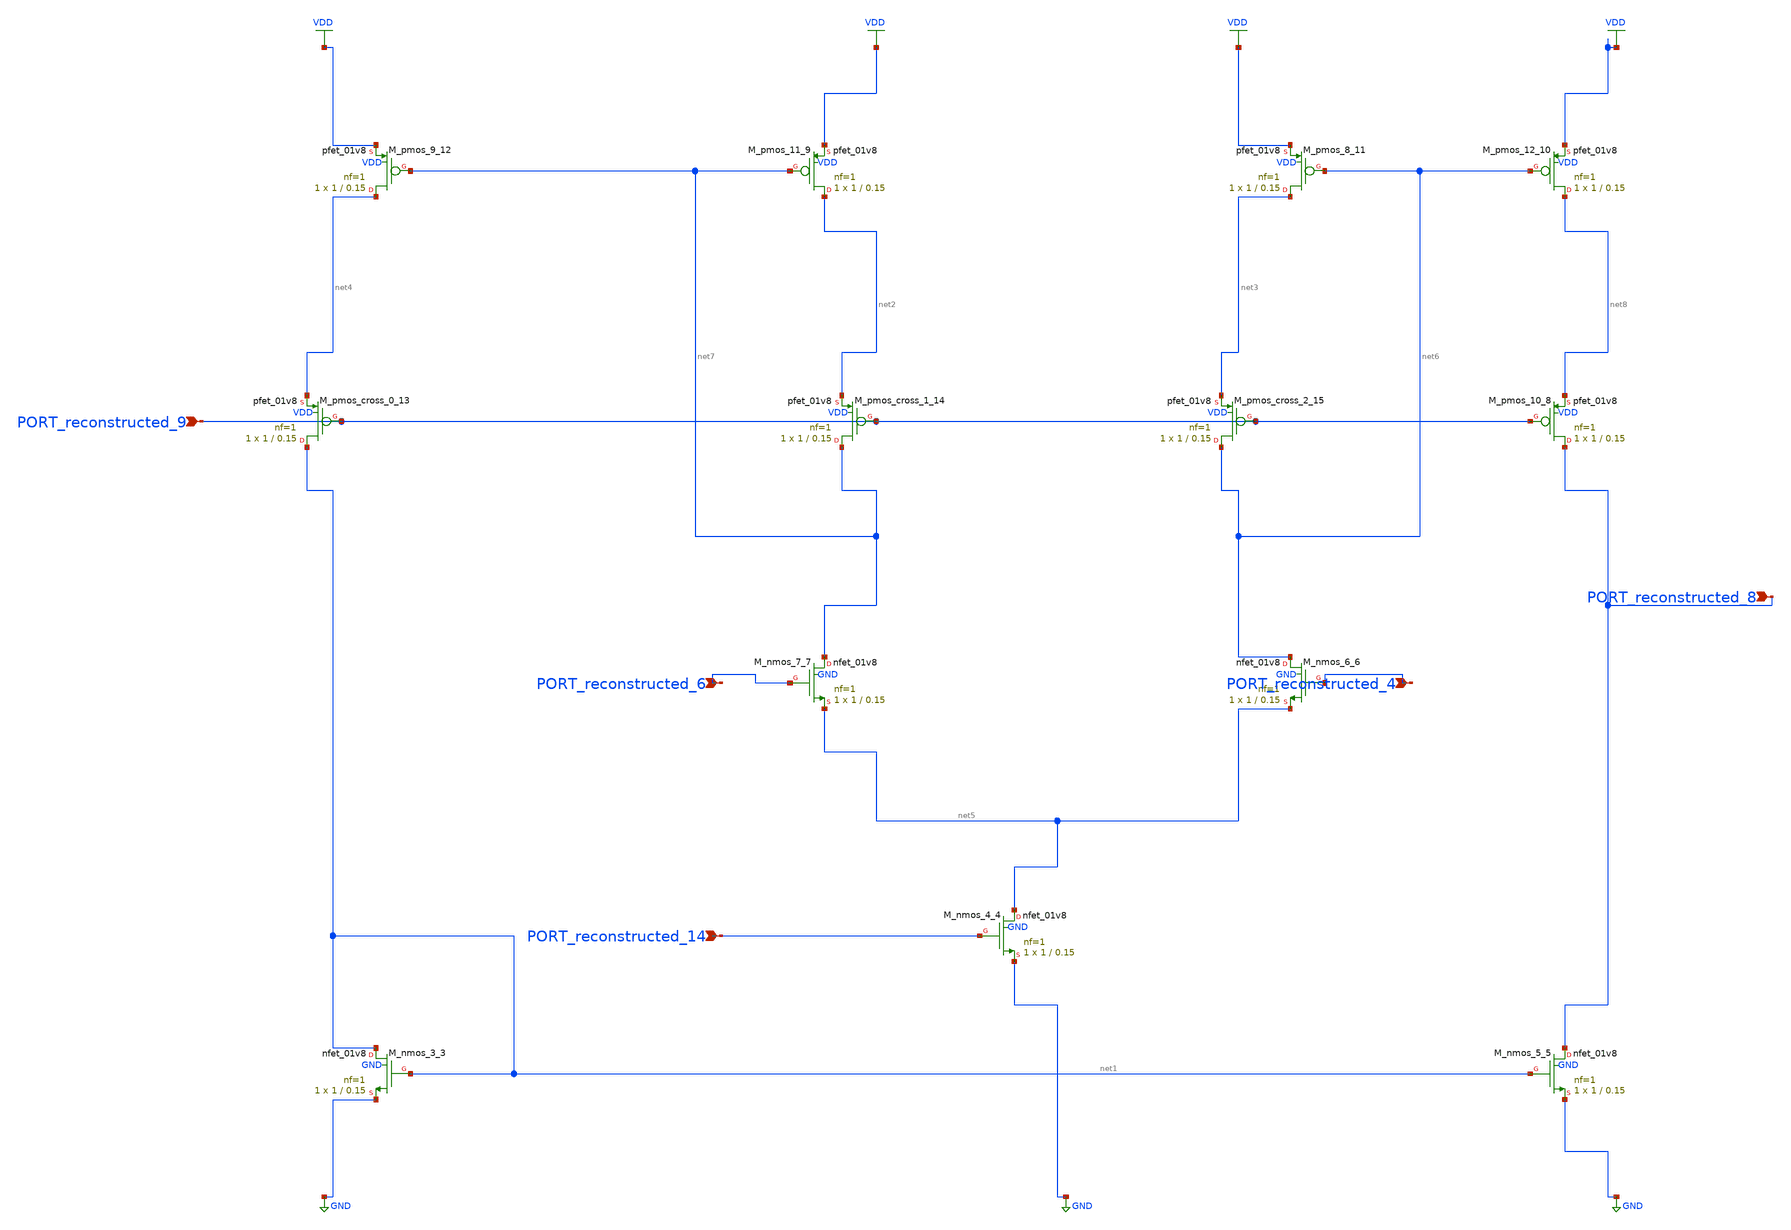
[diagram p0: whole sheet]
** sch_path: schematics/10_1007_BF02104746_102_002.sch
**.subckt 10_1007_BF02104746_102_002 PORT_reconstructed_6 PORT_reconstructed_8 PORT_reconstructed_14
*+ PORT_reconstructed_4 PORT_reconstructed_9
*.ipin PORT_reconstructed_6
*.ipin PORT_reconstructed_8
*.ipin PORT_reconstructed_14
*.ipin PORT_reconstructed_4
*.ipin PORT_reconstructed_9
XM_nmos_3_3 net1 net1 GND GND sky130_fd_pr__nfet_01v8 L=0.15 W=1 nf=1 ad='int((1 + 1)/2) * 1 / 1 * 0.29'
+ as='int((1 + 2)/2) * 1 / 1 * 0.29' pd='2*int((1 + 1)/2) * (1 / 1 + 0.29)' ps='2*int((1 + 2)/2) * (1 / 1 + 0.29)'
+ nrd='0.29 / 1 ' nrs='0.29 / 1 ' sa=0 sb=0 sd=0 mult=1 m=1
XM_nmos_4_4 net5 PORT_reconstructed_14 GND GND sky130_fd_pr__nfet_01v8 L=0.15 W=1 nf=1 ad='int((1 + 1)/2) * 1 / 1 * 0.29'
+ as='int((1 + 2)/2) * 1 / 1 * 0.29' pd='2*int((1 + 1)/2) * (1 / 1 + 0.29)' ps='2*int((1 + 2)/2) * (1 / 1 + 0.29)'
+ nrd='0.29 / 1 ' nrs='0.29 / 1 ' sa=0 sb=0 sd=0 mult=1 m=1
XM_nmos_5_5 PORT_reconstructed_8 net1 GND GND sky130_fd_pr__nfet_01v8 L=0.15 W=1 nf=1 ad='int((1 + 1)/2) * 1 / 1 * 0.29'
+ as='int((1 + 2)/2) * 1 / 1 * 0.29' pd='2*int((1 + 1)/2) * (1 / 1 + 0.29)' ps='2*int((1 + 2)/2) * (1 / 1 + 0.29)'
+ nrd='0.29 / 1 ' nrs='0.29 / 1 ' sa=0 sb=0 sd=0 mult=1 m=1
XM_nmos_6_6 net6 PORT_reconstructed_4 net5 GND sky130_fd_pr__nfet_01v8 L=0.15 W=1 nf=1 ad='int((1 + 1)/2) * 1 / 1 * 0.29'
+ as='int((1 + 2)/2) * 1 / 1 * 0.29' pd='2*int((1 + 1)/2) * (1 / 1 + 0.29)' ps='2*int((1 + 2)/2) * (1 / 1 + 0.29)'
+ nrd='0.29 / 1 ' nrs='0.29 / 1 ' sa=0 sb=0 sd=0 mult=1 m=1
XM_nmos_7_7 net7 PORT_reconstructed_6 net5 GND sky130_fd_pr__nfet_01v8 L=0.15 W=1 nf=1 ad='int((1 + 1)/2) * 1 / 1 * 0.29'
+ as='int((1 + 2)/2) * 1 / 1 * 0.29' pd='2*int((1 + 1)/2) * (1 / 1 + 0.29)' ps='2*int((1 + 2)/2) * (1 / 1 + 0.29)'
+ nrd='0.29 / 1 ' nrs='0.29 / 1 ' sa=0 sb=0 sd=0 mult=1 m=1
XM_pmos_10_8 PORT_reconstructed_8 PORT_reconstructed_9 net8 VDD sky130_fd_pr__pfet_01v8 L=0.15 W=1 nf=1
+ ad='int((1 + 1)/2) * 1 / 1 * 0.29' as='int((1 + 2)/2) * 1 / 1 * 0.29' pd='2*int((1 + 1)/2) * (1 / 1 + 0.29)'
+ ps='2*int((1 + 2)/2) * (1 / 1 + 0.29)' nrd='0.29 / 1 ' nrs='0.29 / 1 ' sa=0 sb=0 sd=0 mult=1 m=1
XM_pmos_11_9 net2 net7 VDD VDD sky130_fd_pr__pfet_01v8 L=0.15 W=1 nf=1 ad='int((1 + 1)/2) * 1 / 1 * 0.29'
+ as='int((1 + 2)/2) * 1 / 1 * 0.29' pd='2*int((1 + 1)/2) * (1 / 1 + 0.29)' ps='2*int((1 + 2)/2) * (1 / 1 + 0.29)'
+ nrd='0.29 / 1 ' nrs='0.29 / 1 ' sa=0 sb=0 sd=0 mult=1 m=1
XM_pmos_12_10 net8 net6 VDD VDD sky130_fd_pr__pfet_01v8 L=0.15 W=1 nf=1 ad='int((1 + 1)/2) * 1 / 1 * 0.29'
+ as='int((1 + 2)/2) * 1 / 1 * 0.29' pd='2*int((1 + 1)/2) * (1 / 1 + 0.29)' ps='2*int((1 + 2)/2) * (1 / 1 + 0.29)'
+ nrd='0.29 / 1 ' nrs='0.29 / 1 ' sa=0 sb=0 sd=0 mult=1 m=1
XM_pmos_8_11 net3 net6 VDD VDD sky130_fd_pr__pfet_01v8 L=0.15 W=1 nf=1 ad='int((1 + 1)/2) * 1 / 1 * 0.29'
+ as='int((1 + 2)/2) * 1 / 1 * 0.29' pd='2*int((1 + 1)/2) * (1 / 1 + 0.29)' ps='2*int((1 + 2)/2) * (1 / 1 + 0.29)'
+ nrd='0.29 / 1 ' nrs='0.29 / 1 ' sa=0 sb=0 sd=0 mult=1 m=1
XM_pmos_9_12 net4 net7 VDD VDD sky130_fd_pr__pfet_01v8 L=0.15 W=1 nf=1 ad='int((1 + 1)/2) * 1 / 1 * 0.29'
+ as='int((1 + 2)/2) * 1 / 1 * 0.29' pd='2*int((1 + 1)/2) * (1 / 1 + 0.29)' ps='2*int((1 + 2)/2) * (1 / 1 + 0.29)'
+ nrd='0.29 / 1 ' nrs='0.29 / 1 ' sa=0 sb=0 sd=0 mult=1 m=1
XM_pmos_cross_0_13 net1 PORT_reconstructed_9 net4 VDD sky130_fd_pr__pfet_01v8 L=0.15 W=1 nf=1 ad='int((1 + 1)/2) * 1 / 1 * 0.29'
+ as='int((1 + 2)/2) * 1 / 1 * 0.29' pd='2*int((1 + 1)/2) * (1 / 1 + 0.29)' ps='2*int((1 + 2)/2) * (1 / 1 + 0.29)'
+ nrd='0.29 / 1 ' nrs='0.29 / 1 ' sa=0 sb=0 sd=0 mult=1 m=1
XM_pmos_cross_1_14 net7 PORT_reconstructed_9 net2 VDD sky130_fd_pr__pfet_01v8 L=0.15 W=1 nf=1 ad='int((1 + 1)/2) * 1 / 1 * 0.29'
+ as='int((1 + 2)/2) * 1 / 1 * 0.29' pd='2*int((1 + 1)/2) * (1 / 1 + 0.29)' ps='2*int((1 + 2)/2) * (1 / 1 + 0.29)'
+ nrd='0.29 / 1 ' nrs='0.29 / 1 ' sa=0 sb=0 sd=0 mult=1 m=1
XM_pmos_cross_2_15 net6 PORT_reconstructed_9 net3 VDD sky130_fd_pr__pfet_01v8 L=0.15 W=1 nf=1 ad='int((1 + 1)/2) * 1 / 1 * 0.29'
+ as='int((1 + 2)/2) * 1 / 1 * 0.29' pd='2*int((1 + 1)/2) * (1 / 1 + 0.29)' ps='2*int((1 + 2)/2) * (1 / 1 + 0.29)'
+ nrd='0.29 / 1 ' nrs='0.29 / 1 ' sa=0 sb=0 sd=0 mult=1 m=1
**.ends
.GLOBAL GND
.GLOBAL VDD
.end
